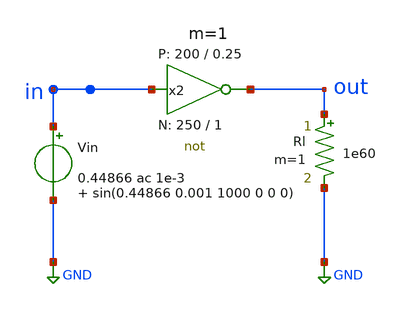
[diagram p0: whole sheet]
** sch_path: Amplifier_Inv/xschem/untitled.sch
* StefanSchippers/xschem_sky130/sky130_tests/not.sch:
* Copyright 2021 Stefan Frederik Schippers
* Licensed under the Apache License, Version 2.0 (the "License");
**.subckt untitled
x2 out in VCC VSS not W_N=250 L_N=1 W_P=200 L_P=0.25 m=1
Vin in GND 0.44866 ac 1e-3 sin(0.44866 0.001 1000 0 0 0)
Rl out GND 1e60 m=1
**** begin user architecture code

** opencircuitdesign pdks install
.lib $::SKYWATER_MODELS/sky130.lib.spice tt



.control

  dc Vin 0 1.125 0.00001
  save all v(out)
  write little_test.raw v(out)

  exit 0
.endc


**** end user architecture code
**.ends

* expanding   symbol:  sky130_tests/not.sym # of pins=2
** sym_path: sky130_tests/not.sym
** sch_path: sky130_tests/not.sch
.subckt not y a VCCPIN VSSPIN     W_N=1 L_N=0.15 W_P=2 L_P=0.15
*.opin y
*.ipin a
XM1 DN a VSSPIN VSSPIN sky130_fd_pr__nfet_01v8 L=L_N W=W_N nf=1 ad='int((1 + 1)/2) * W_N / 1 * 0.29'
+ as='int((1 + 2)/2) * W_N / 1 * 0.29' pd='2*int((1 + 1)/2) * (W_N / 1 + 0.29)' ps='2*int((1 + 2)/2) * (W_N / 1 + 0.29)'
+ nrd='0.29 / W_N ' nrs='0.29 / W_N ' sa=0 sb=0 sd=0 mult=1 m=1
XM2 DP a VCCPIN VCCPIN sky130_fd_pr__pfet_01v8 L=L_P W=W_P nf=1 ad='int((nf+1)/2) * W/nf * 0.29' as='int((nf+2)/2) * W/nf * 0.29'
+ pd='2*int((nf+1)/2) * (W/nf + 0.29)' ps='2*int((nf+2)/2) * (W/nf + 0.29)' nrd='0.29 / W' nrs='0.29 / W'
+ sa=0 sb=0 sd=0 mult=1 m=1
Vmeas DP y 0
.save i(vmeas)
Vmeas1 y DN 0
.save i(vmeas1)
.save v(dp)
.save v(dn)
.ends

.GLOBAL GND
.end
